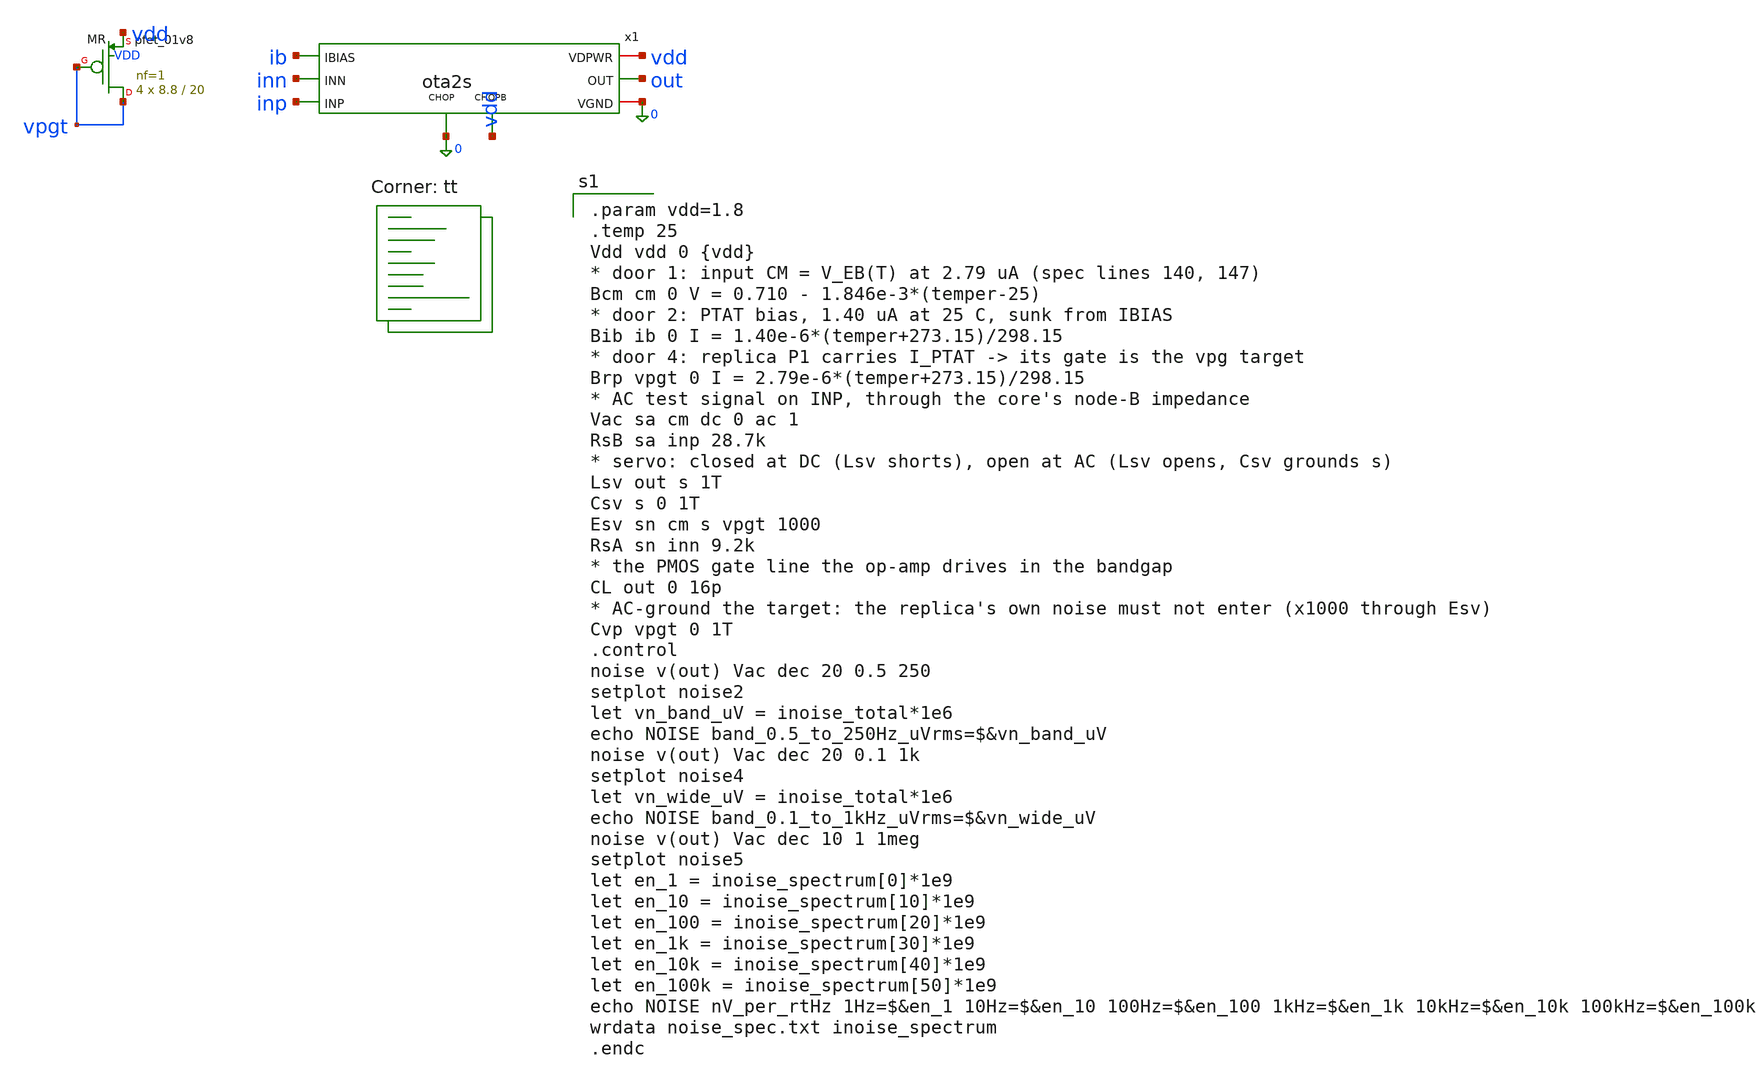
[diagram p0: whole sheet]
** sch_path: xschem/tb_ota2s_noise.sch
**.subckt tb_ota2s_noise
x1 inp inn out vdd 0 ib 0 vdd ota2s
XMR vpgt vpgt vdd VDD sky130_fd_pr__pfet_01v8 L=20 W=8.8 nf=1 ad='int((1 + 1)/2) * 8.8 / 1 * 0.29' as='int((1 + 2)/2) * 8.8 / 1 * 0.29'
+ pd='2*int((1 + 1)/2) * (8.8 / 1 + 0.29)' ps='2*int((1 + 2)/2) * (8.8 / 1 + 0.29)' nrd='0.29 / 8.8 ' nrs='0.29 / 8.8 '
+ sa=0 sb=0 sd=0 mult=4 m=4
**** begin user architecture code
.lib $::SKYWATER_MODELS/sky130.lib.spice tt

.param vdd=1.8
.temp 25
Vdd vdd 0 {vdd}
* door 1: input CM = V_EB(T) at 2.79 uA (spec lines 140, 147)
Bcm cm 0 V = 0.710 - 1.846e-3*(temper-25)
* door 2: PTAT bias, 1.40 uA at 25 C, sunk from IBIAS
Bib ib 0 I = 1.40e-6*(temper+273.15)/298.15
* door 4: replica P1 carries I_PTAT -> its gate is the vpg target
Brp vpgt 0 I = 2.79e-6*(temper+273.15)/298.15
* AC test signal on INP, through the core's node-B impedance
Vac sa cm dc 0 ac 1
RsB sa inp 28.7k
* servo: closed at DC (Lsv shorts), open at AC (Lsv opens, Csv grounds s)
Lsv out s 1T
Csv s 0 1T
Esv sn cm s vpgt 1000
RsA sn inn 9.2k
* the PMOS gate line the op-amp drives in the bandgap
CL out 0 16p
* AC-ground the target: the replica's own noise must not enter (x1000 through Esv)
Cvp vpgt 0 1T
.control
noise v(out) Vac dec 20 0.5 250
setplot noise2
let vn_band_uV = inoise_total*1e6
echo NOISE band_0.5_to_250Hz_uVrms=$&vn_band_uV
noise v(out) Vac dec 20 0.1 1k
setplot noise4
let vn_wide_uV = inoise_total*1e6
echo NOISE band_0.1_to_1kHz_uVrms=$&vn_wide_uV
noise v(out) Vac dec 10 1 1meg
setplot noise5
let en_1 = inoise_spectrum[0]*1e9
let en_10 = inoise_spectrum[10]*1e9
let en_100 = inoise_spectrum[20]*1e9
let en_1k = inoise_spectrum[30]*1e9
let en_10k = inoise_spectrum[40]*1e9
let en_100k = inoise_spectrum[50]*1e9
echo NOISE nV_per_rtHz 1Hz=$&en_1 10Hz=$&en_10 100Hz=$&en_100 1kHz=$&en_1k 10kHz=$&en_10k
+ 100kHz=$&en_100k
wrdata noise_spec.txt inoise_spectrum
.endc

**** end user architecture code
**.ends

* expanding   symbol:  ota2s.sym # of pins=8
** sym_path: xschem/ota2s.sym
** sch_path: xschem/ota2s.sch
.subckt ota2s INP INN OUT VDPWR VGND IBIAS CHOP CHOPB
*.ipin INN
*.ipin INP
*.ipin IBIAS
*.opin OUT
*.iopin VDPWR
*.iopin VGND
*.ipin CHOPB
*.ipin CHOP
XMREF IBIAS IBIAS VDPWR VDPWR sky130_fd_pr__pfet_01v8 L=4 W=20 nf=1 ad='int((1 + 1)/2) * 20 / 1 * 0.29'
+ as='int((1 + 2)/2) * 20 / 1 * 0.29' pd='2*int((1 + 1)/2) * (20 / 1 + 0.29)' ps='2*int((1 + 2)/2) * (20 / 1 + 0.29)'
+ nrd='0.29 / 20 ' nrs='0.29 / 20 ' sa=0 sb=0 sd=0 mult=1 m=1
XMTAIL tail IBIAS VDPWR VDPWR sky130_fd_pr__pfet_01v8 L=4 W=20 nf=1 ad='int((1 + 1)/2) * 20 / 1 * 0.29'
+ as='int((1 + 2)/2) * 20 / 1 * 0.29' pd='2*int((1 + 1)/2) * (20 / 1 + 0.29)' ps='2*int((1 + 2)/2) * (20 / 1 + 0.29)'
+ nrd='0.29 / 20 ' nrs='0.29 / 20 ' sa=0 sb=0 sd=0 mult=2 m=2
XMP1 d1 INN tail VDPWR sky130_fd_pr__pfet_01v8_lvt L=6 W=25 nf=1 ad='int((1 + 1)/2) * 25 / 1 * 0.29'
+ as='int((1 + 2)/2) * 25 / 1 * 0.29' pd='2*int((1 + 1)/2) * (25 / 1 + 0.29)' ps='2*int((1 + 2)/2) * (25 / 1 + 0.29)'
+ nrd='0.29 / 25 ' nrs='0.29 / 25 ' sa=0 sb=0 sd=0 mult=24 m=24
XMP2 x1 INP tail VDPWR sky130_fd_pr__pfet_01v8_lvt L=6 W=25 nf=1 ad='int((1 + 1)/2) * 25 / 1 * 0.29'
+ as='int((1 + 2)/2) * 25 / 1 * 0.29' pd='2*int((1 + 1)/2) * (25 / 1 + 0.29)' ps='2*int((1 + 2)/2) * (25 / 1 + 0.29)'
+ nrd='0.29 / 25 ' nrs='0.29 / 25 ' sa=0 sb=0 sd=0 mult=24 m=24
XMN1 d1 g12 VGND VGND sky130_fd_pr__nfet_01v8 L=20 W=6 nf=1 ad='int((1 + 1)/2) * 6 / 1 * 0.29' as='int((1 + 2)/2) * 6 / 1 * 0.29'
+ pd='2*int((1 + 1)/2) * (6 / 1 + 0.29)' ps='2*int((1 + 2)/2) * (6 / 1 + 0.29)' nrd='0.29 / 6 ' nrs='0.29 / 6 '
+ sa=0 sb=0 sd=0 mult=2 m=2
XMN2 x1 g12 VGND VGND sky130_fd_pr__nfet_01v8 L=20 W=6 nf=1 ad='int((1 + 1)/2) * 6 / 1 * 0.29' as='int((1 + 2)/2) * 6 / 1 * 0.29'
+ pd='2*int((1 + 1)/2) * (6 / 1 + 0.29)' ps='2*int((1 + 2)/2) * (6 / 1 + 0.29)' nrd='0.29 / 6 ' nrs='0.29 / 6 '
+ sa=0 sb=0 sd=0 mult=2 m=2
XMP3 OUT IBIAS VDPWR VDPWR sky130_fd_pr__pfet_01v8 L=4 W=20 nf=1 ad='int((1 + 1)/2) * 20 / 1 * 0.29'
+ as='int((1 + 2)/2) * 20 / 1 * 0.29' pd='2*int((1 + 1)/2) * (20 / 1 + 0.29)' ps='2*int((1 + 2)/2) * (20 / 1 + 0.29)'
+ nrd='0.29 / 20 ' nrs='0.29 / 20 ' sa=0 sb=0 sd=0 mult=6 m=6
XMN3 OUT g3 VGND VGND sky130_fd_pr__nfet_01v8 L=1 W=7 nf=1 ad='int((1 + 1)/2) * 7 / 1 * 0.29' as='int((1 + 2)/2) * 7 / 1 * 0.29'
+ pd='2*int((1 + 1)/2) * (7 / 1 + 0.29)' ps='2*int((1 + 2)/2) * (7 / 1 + 0.29)' nrd='0.29 / 7 ' nrs='0.29 / 7 '
+ sa=0 sb=0 sd=0 mult=1 m=1
XRZ1 net1 g3 VGND sky130_fd_pr__res_high_po_1p41 L=20 mult=1 m=1
XRZ2 net2 net1 VGND sky130_fd_pr__res_high_po_1p41 L=20 mult=1 m=1
XRZ3 net3 net2 VGND sky130_fd_pr__res_high_po_1p41 L=20 mult=1 m=1
XRZ4 net4 net3 VGND sky130_fd_pr__res_high_po_1p41 L=20 mult=1 m=1
XRZ5 net5 net4 VGND sky130_fd_pr__res_high_po_1p41 L=20 mult=1 m=1
XRZ6 cz net5 VGND sky130_fd_pr__res_high_po_1p41 L=20 mult=1 m=1
XCC cz OUT sky130_fd_pr__cap_mim_m3_1 W=25 L=25 MF=8 m=8
XDP tail VDPWR tail VDPWR sky130_fd_pr__pfet_01v8_lvt L=6 W=25 nf=1 ad='int((1 + 1)/2) * 25 / 1 * 0.29'
+ as='int((1 + 2)/2) * 25 / 1 * 0.29' pd='2*int((1 + 1)/2) * (25 / 1 + 0.29)' ps='2*int((1 + 2)/2) * (25 / 1 + 0.29)'
+ nrd='0.29 / 25 ' nrs='0.29 / 25 ' sa=0 sb=0 sd=0 mult=8 m=8
XDNA d1 VGND VGND VGND sky130_fd_pr__nfet_01v8 L=20 W=6 nf=1 ad='int((1 + 1)/2) * 6 / 1 * 0.29' as='int((1 + 2)/2) * 6 / 1 * 0.29'
+ pd='2*int((1 + 1)/2) * (6 / 1 + 0.29)' ps='2*int((1 + 2)/2) * (6 / 1 + 0.29)' nrd='0.29 / 6 ' nrs='0.29 / 6 '
+ sa=0 sb=0 sd=0 mult=2 m=2
XDNB x1 VGND VGND VGND sky130_fd_pr__nfet_01v8 L=20 W=6 nf=1 ad='int((1 + 1)/2) * 6 / 1 * 0.29' as='int((1 + 2)/2) * 6 / 1 * 0.29'
+ pd='2*int((1 + 1)/2) * (6 / 1 + 0.29)' ps='2*int((1 + 2)/2) * (6 / 1 + 0.29)' nrd='0.29 / 6 ' nrs='0.29 / 6 '
+ sa=0 sb=0 sd=0 mult=2 m=2
XDB VDPWR VDPWR VDPWR VDPWR sky130_fd_pr__pfet_01v8 L=4 W=20 nf=1 ad='int((1 + 1)/2) * 20 / 1 * 0.29'
+ as='int((1 + 2)/2) * 20 / 1 * 0.29' pd='2*int((1 + 1)/2) * (20 / 1 + 0.29)' ps='2*int((1 + 2)/2) * (20 / 1 + 0.29)'
+ nrd='0.29 / 20 ' nrs='0.29 / 20 ' sa=0 sb=0 sd=0 mult=2 m=2
XRD1 VGND VGND VGND sky130_fd_pr__res_high_po_1p41 L=20 mult=1 m=1
XRD2 VGND VGND VGND sky130_fd_pr__res_high_po_1p41 L=20 mult=1 m=1
XSD1 d1 CHOPB g12 VGND sky130_fd_pr__nfet_01v8 L=0.5 W=6 nf=1 ad='int((1 + 1)/2) * 6 / 1 * 0.29' as='int((1 + 2)/2) * 6 / 1 * 0.29'
+ pd='2*int((1 + 1)/2) * (6 / 1 + 0.29)' ps='2*int((1 + 2)/2) * (6 / 1 + 0.29)' nrd='0.29 / 6 ' nrs='0.29 / 6 '
+ sa=0 sb=0 sd=0 mult=1 m=1
XSD2 x1 CHOP g12 VGND sky130_fd_pr__nfet_01v8 L=0.5 W=6 nf=1 ad='int((1 + 1)/2) * 6 / 1 * 0.29' as='int((1 + 2)/2) * 6 / 1 * 0.29'
+ pd='2*int((1 + 1)/2) * (6 / 1 + 0.29)' ps='2*int((1 + 2)/2) * (6 / 1 + 0.29)' nrd='0.29 / 6 ' nrs='0.29 / 6 '
+ sa=0 sb=0 sd=0 mult=1 m=1
XSG2 g3 CHOP d1 VGND sky130_fd_pr__nfet_01v8 L=0.5 W=6 nf=1 ad='int((1 + 1)/2) * 6 / 1 * 0.29' as='int((1 + 2)/2) * 6 / 1 * 0.29'
+ pd='2*int((1 + 1)/2) * (6 / 1 + 0.29)' ps='2*int((1 + 2)/2) * (6 / 1 + 0.29)' nrd='0.29 / 6 ' nrs='0.29 / 6 '
+ sa=0 sb=0 sd=0 mult=1 m=1
XSG1 x1 CHOPB g3 VGND sky130_fd_pr__nfet_01v8 L=0.5 W=6 nf=1 ad='int((1 + 1)/2) * 6 / 1 * 0.29' as='int((1 + 2)/2) * 6 / 1 * 0.29'
+ pd='2*int((1 + 1)/2) * (6 / 1 + 0.29)' ps='2*int((1 + 2)/2) * (6 / 1 + 0.29)' nrd='0.29 / 6 ' nrs='0.29 / 6 '
+ sa=0 sb=0 sd=0 mult=1 m=1
.ends

.end
